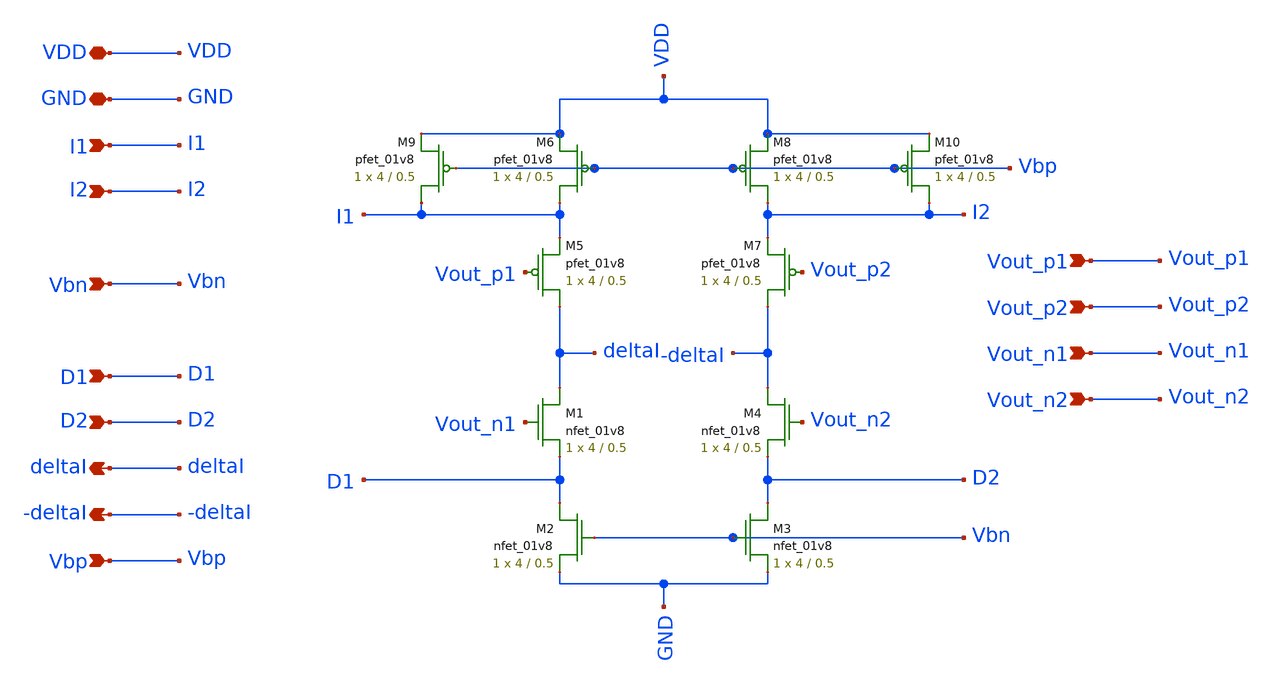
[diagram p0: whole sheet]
** sch_path: final/LDS/summation_LDS.sch
**.subckt summation_LDS VDD GND I1 I2 Vbn D1 D2 deltaI -deltaI Vbp Vout_p1 Vout_p2 Vout_n1 Vout_n2
*.iopin VDD
*.iopin GND
*.ipin I1
*.ipin I2
*.ipin Vbn
*.ipin D1
*.ipin D2
*.opin deltaI
*.opin -deltaI
*.ipin Vbp
*.ipin Vout_p1
*.ipin Vout_p2
*.ipin Vout_n1
*.ipin Vout_n2
XM1 deltaI Vout_n1 D1 GND sky130_fd_pr__nfet_01v8 L=0.5 W=4 nf=1 ad='int((nf+1)/2) * W/nf * 0.29' as='int((nf+2)/2) * W/nf * 0.29'
+ pd='2*int((nf+1)/2) * (W/nf + 0.29)' ps='2*int((nf+2)/2) * (W/nf + 0.29)' nrd='0.29 / W' nrs='0.29 / W'
+ sa=0 sb=0 sd=0 mult=1 m=1
XM9 I1 Vbp VDD VDD sky130_fd_pr__pfet_01v8 L=0.5 W=4 nf=1 ad='int((nf+1)/2) * W/nf * 0.29' as='int((nf+2)/2) * W/nf * 0.29'
+ pd='2*int((nf+1)/2) * (W/nf + 0.29)' ps='2*int((nf+2)/2) * (W/nf + 0.29)' nrd='0.29 / W' nrs='0.29 / W'
+ sa=0 sb=0 sd=0 mult=1 m=1
XM6 I1 Vbp VDD VDD sky130_fd_pr__pfet_01v8 L=0.5 W=4 nf=1 ad='int((nf+1)/2) * W/nf * 0.29' as='int((nf+2)/2) * W/nf * 0.29'
+ pd='2*int((nf+1)/2) * (W/nf + 0.29)' ps='2*int((nf+2)/2) * (W/nf + 0.29)' nrd='0.29 / W' nrs='0.29 / W'
+ sa=0 sb=0 sd=0 mult=1 m=1
XM8 I2 Vbp VDD VDD sky130_fd_pr__pfet_01v8 L=0.5 W=4 nf=1 ad='int((nf+1)/2) * W/nf * 0.29' as='int((nf+2)/2) * W/nf * 0.29'
+ pd='2*int((nf+1)/2) * (W/nf + 0.29)' ps='2*int((nf+2)/2) * (W/nf + 0.29)' nrd='0.29 / W' nrs='0.29 / W'
+ sa=0 sb=0 sd=0 mult=1 m=1
XM10 I2 Vbp VDD VDD sky130_fd_pr__pfet_01v8 L=0.5 W=4 nf=1 ad='int((nf+1)/2) * W/nf * 0.29' as='int((nf+2)/2) * W/nf * 0.29'
+ pd='2*int((nf+1)/2) * (W/nf + 0.29)' ps='2*int((nf+2)/2) * (W/nf + 0.29)' nrd='0.29 / W' nrs='0.29 / W'
+ sa=0 sb=0 sd=0 mult=1 m=1
XM5 deltaI Vout_p1 I1 VDD sky130_fd_pr__pfet_01v8 L=0.5 W=4 nf=1 ad='int((nf+1)/2) * W/nf * 0.29' as='int((nf+2)/2) * W/nf * 0.29'
+ pd='2*int((nf+1)/2) * (W/nf + 0.29)' ps='2*int((nf+2)/2) * (W/nf + 0.29)' nrd='0.29 / W' nrs='0.29 / W'
+ sa=0 sb=0 sd=0 mult=1 m=1
XM7 -deltaI Vout_p2 I2 VDD sky130_fd_pr__pfet_01v8 L=0.5 W=4 nf=1 ad='int((nf+1)/2) * W/nf * 0.29' as='int((nf+2)/2) * W/nf * 0.29'
+ pd='2*int((nf+1)/2) * (W/nf + 0.29)' ps='2*int((nf+2)/2) * (W/nf + 0.29)' nrd='0.29 / W' nrs='0.29 / W'
+ sa=0 sb=0 sd=0 mult=1 m=1
XM2 D1 Vbn GND GND sky130_fd_pr__nfet_01v8 L=0.5 W=4 nf=1 ad='int((nf+1)/2) * W/nf * 0.29' as='int((nf+2)/2) * W/nf * 0.29'
+ pd='2*int((nf+1)/2) * (W/nf + 0.29)' ps='2*int((nf+2)/2) * (W/nf + 0.29)' nrd='0.29 / W' nrs='0.29 / W'
+ sa=0 sb=0 sd=0 mult=1 m=1
XM3 D2 Vbn GND GND sky130_fd_pr__nfet_01v8 L=0.5 W=4 nf=1 ad='int((nf+1)/2) * W/nf * 0.29' as='int((nf+2)/2) * W/nf * 0.29'
+ pd='2*int((nf+1)/2) * (W/nf + 0.29)' ps='2*int((nf+2)/2) * (W/nf + 0.29)' nrd='0.29 / W' nrs='0.29 / W'
+ sa=0 sb=0 sd=0 mult=1 m=1
XM4 -deltaI Vout_n2 D2 GND sky130_fd_pr__nfet_01v8 L=0.5 W=4 nf=1 ad='int((nf+1)/2) * W/nf * 0.29' as='int((nf+2)/2) * W/nf * 0.29'
+ pd='2*int((nf+1)/2) * (W/nf + 0.29)' ps='2*int((nf+2)/2) * (W/nf + 0.29)' nrd='0.29 / W' nrs='0.29 / W'
+ sa=0 sb=0 sd=0 mult=1 m=1
**.ends
.end
